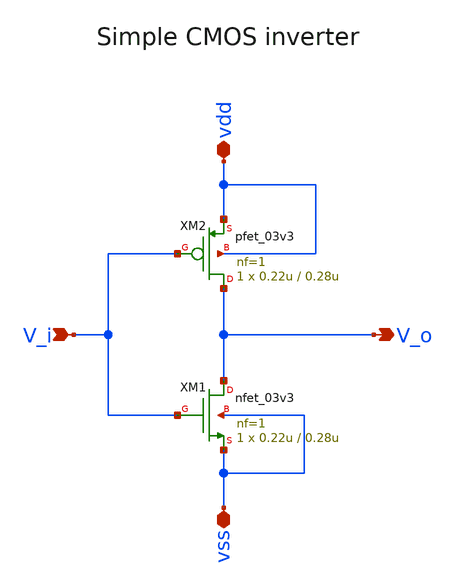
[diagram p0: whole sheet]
** sch_path: designs/test/test-inv.sch
**.subckt test-inv vdd vss V_i V_o
*.iopin vdd
*.iopin vss
*.ipin V_i
*.opin V_o
XM1 V_o V_i vss vss nfet_03v3 L=0.28u W=0.22u nf=1 ad='int((nf+1)/2) * W/nf * 0.18u' as='int((nf+2)/2) * W/nf * 0.18u'
+ pd='2*int((nf+1)/2) * (W/nf + 0.18u)' ps='2*int((nf+2)/2) * (W/nf + 0.18u)' nrd='0.18u / W' nrs='0.18u / W'
+ sa=0 sb=0 sd=0 m=1
XM2 V_o V_i vdd vdd pfet_03v3 L=0.28u W=0.22u nf=1 ad='int((nf+1)/2) * W/nf * 0.18u' as='int((nf+2)/2) * W/nf * 0.18u'
+ pd='2*int((nf+1)/2) * (W/nf + 0.18u)' ps='2*int((nf+2)/2) * (W/nf + 0.18u)' nrd='0.18u / W' nrs='0.18u / W'
+ sa=0 sb=0 sd=0 m=1
**.ends
.end
